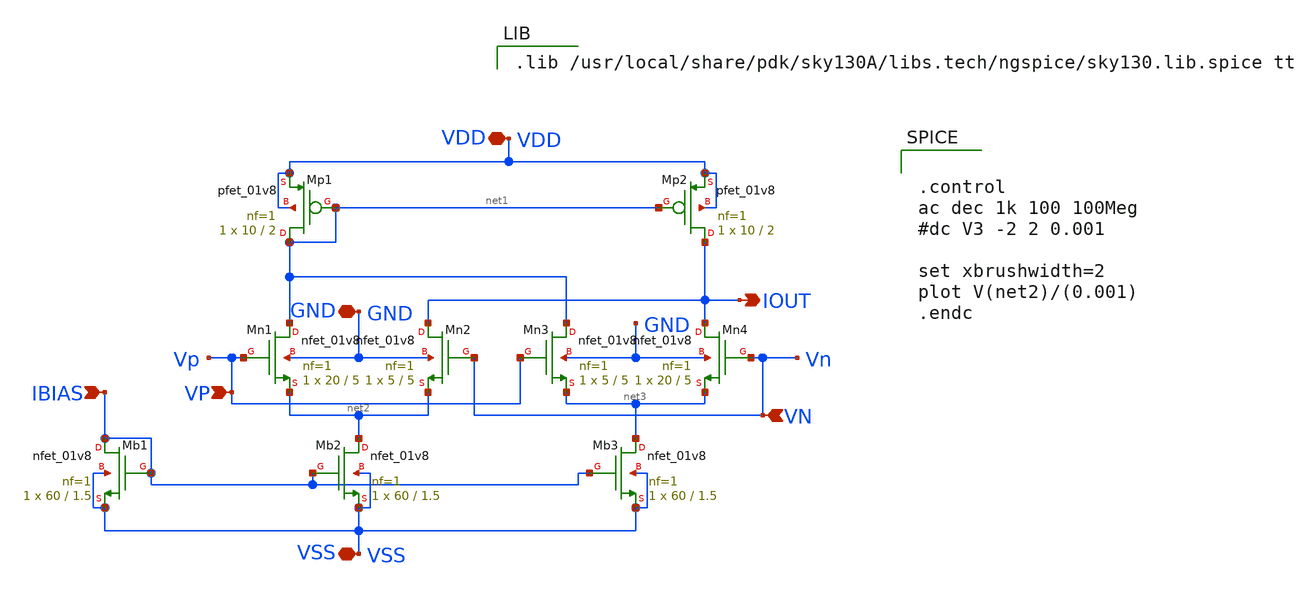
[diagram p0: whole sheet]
** sch_path: ANALOG_FOPID_XSCHEM/OTA/ota3.sch
**.subckt ota3 VP IBIAS IOUT VDD VSS VN GND
*.ipin VP
*.ipin IBIAS
*.opin IOUT
*.iopin VDD
*.iopin VSS
*.ipin VN
*.iopin GND
XMp1 net1 net1 VDD VDD sky130_fd_pr__pfet_01v8 L=2 W=10 nf=1 ad='int((nf+1)/2) * W/nf * 0.29' as='int((nf+2)/2) * W/nf * 0.29'
+ pd='2*int((nf+1)/2) * (W/nf + 0.29)' ps='2*int((nf+2)/2) * (W/nf + 0.29)' nrd='0.29 / W' nrs='0.29 / W'
+ sa=0 sb=0 sd=0 mult=1 m=1
XMp2 IOUT net1 VDD VDD sky130_fd_pr__pfet_01v8 L=2 W=10 nf=1 ad='int((nf+1)/2) * W/nf * 0.29' as='int((nf+2)/2) * W/nf * 0.29'
+ pd='2*int((nf+1)/2) * (W/nf + 0.29)' ps='2*int((nf+2)/2) * (W/nf + 0.29)' nrd='0.29 / W' nrs='0.29 / W'
+ sa=0 sb=0 sd=0 mult=1 m=1
XMn1 net1 Vp net2 GND sky130_fd_pr__nfet_01v8 L=5 W=20 nf=1 ad='int((nf+1)/2) * W/nf * 0.29' as='int((nf+2)/2) * W/nf * 0.29'
+ pd='2*int((nf+1)/2) * (W/nf + 0.29)' ps='2*int((nf+2)/2) * (W/nf + 0.29)' nrd='0.29 / W' nrs='0.29 / W'
+ sa=0 sb=0 sd=0 mult=1 m=1
XMn2 IOUT Vn net2 GND sky130_fd_pr__nfet_01v8 L=5 W=5 nf=1 ad='int((nf+1)/2) * W/nf * 0.29' as='int((nf+2)/2) * W/nf * 0.29'
+ pd='2*int((nf+1)/2) * (W/nf + 0.29)' ps='2*int((nf+2)/2) * (W/nf + 0.29)' nrd='0.29 / W' nrs='0.29 / W'
+ sa=0 sb=0 sd=0 mult=1 m=1
XMn3 net1 Vp net3 GND sky130_fd_pr__nfet_01v8 L=5 W=5 nf=1 ad='int((nf+1)/2) * W/nf * 0.29' as='int((nf+2)/2) * W/nf * 0.29'
+ pd='2*int((nf+1)/2) * (W/nf + 0.29)' ps='2*int((nf+2)/2) * (W/nf + 0.29)' nrd='0.29 / W' nrs='0.29 / W'
+ sa=0 sb=0 sd=0 mult=1 m=1
XMn4 IOUT Vn net3 GND sky130_fd_pr__nfet_01v8 L=5 W=20 nf=1 ad='int((nf+1)/2) * W/nf * 0.29' as='int((nf+2)/2) * W/nf * 0.29'
+ pd='2*int((nf+1)/2) * (W/nf + 0.29)' ps='2*int((nf+2)/2) * (W/nf + 0.29)' nrd='0.29 / W' nrs='0.29 / W'
+ sa=0 sb=0 sd=0 mult=1 m=1
XMb2 net2 IBIAS VSS VSS sky130_fd_pr__nfet_01v8 L=1.5 W=60 nf=1 ad='int((nf+1)/2) * W/nf * 0.29' as='int((nf+2)/2) * W/nf * 0.29'
+ pd='2*int((nf+1)/2) * (W/nf + 0.29)' ps='2*int((nf+2)/2) * (W/nf + 0.29)' nrd='0.29 / W' nrs='0.29 / W'
+ sa=0 sb=0 sd=0 mult=1 m=1
XMb1 IBIAS IBIAS VSS VSS sky130_fd_pr__nfet_01v8 L=1.5 W=60 nf=1 ad='int((nf+1)/2) * W/nf * 0.29' as='int((nf+2)/2) * W/nf * 0.29'
+ pd='2*int((nf+1)/2) * (W/nf + 0.29)' ps='2*int((nf+2)/2) * (W/nf + 0.29)' nrd='0.29 / W' nrs='0.29 / W'
+ sa=0 sb=0 sd=0 mult=1 m=1
XMb3 net3 IBIAS VSS VSS sky130_fd_pr__nfet_01v8 L=1.5 W=60 nf=1 ad='int((nf+1)/2) * W/nf * 0.29' as='int((nf+2)/2) * W/nf * 0.29'
+ pd='2*int((nf+1)/2) * (W/nf + 0.29)' ps='2*int((nf+2)/2) * (W/nf + 0.29)' nrd='0.29 / W' nrs='0.29 / W'
+ sa=0 sb=0 sd=0 mult=1 m=1
**** begin user architecture code

.lib /usr/local/share/pdk/sky130A/libs.tech/ngspice/sky130.lib.spice tt



.control
ac dec 1k 100 100Meg
#dc V3 -2 2 0.001

set xbrushwidth=2
plot V(net2)/(0.001)
.endc


**** end user architecture code
**.ends
.end
